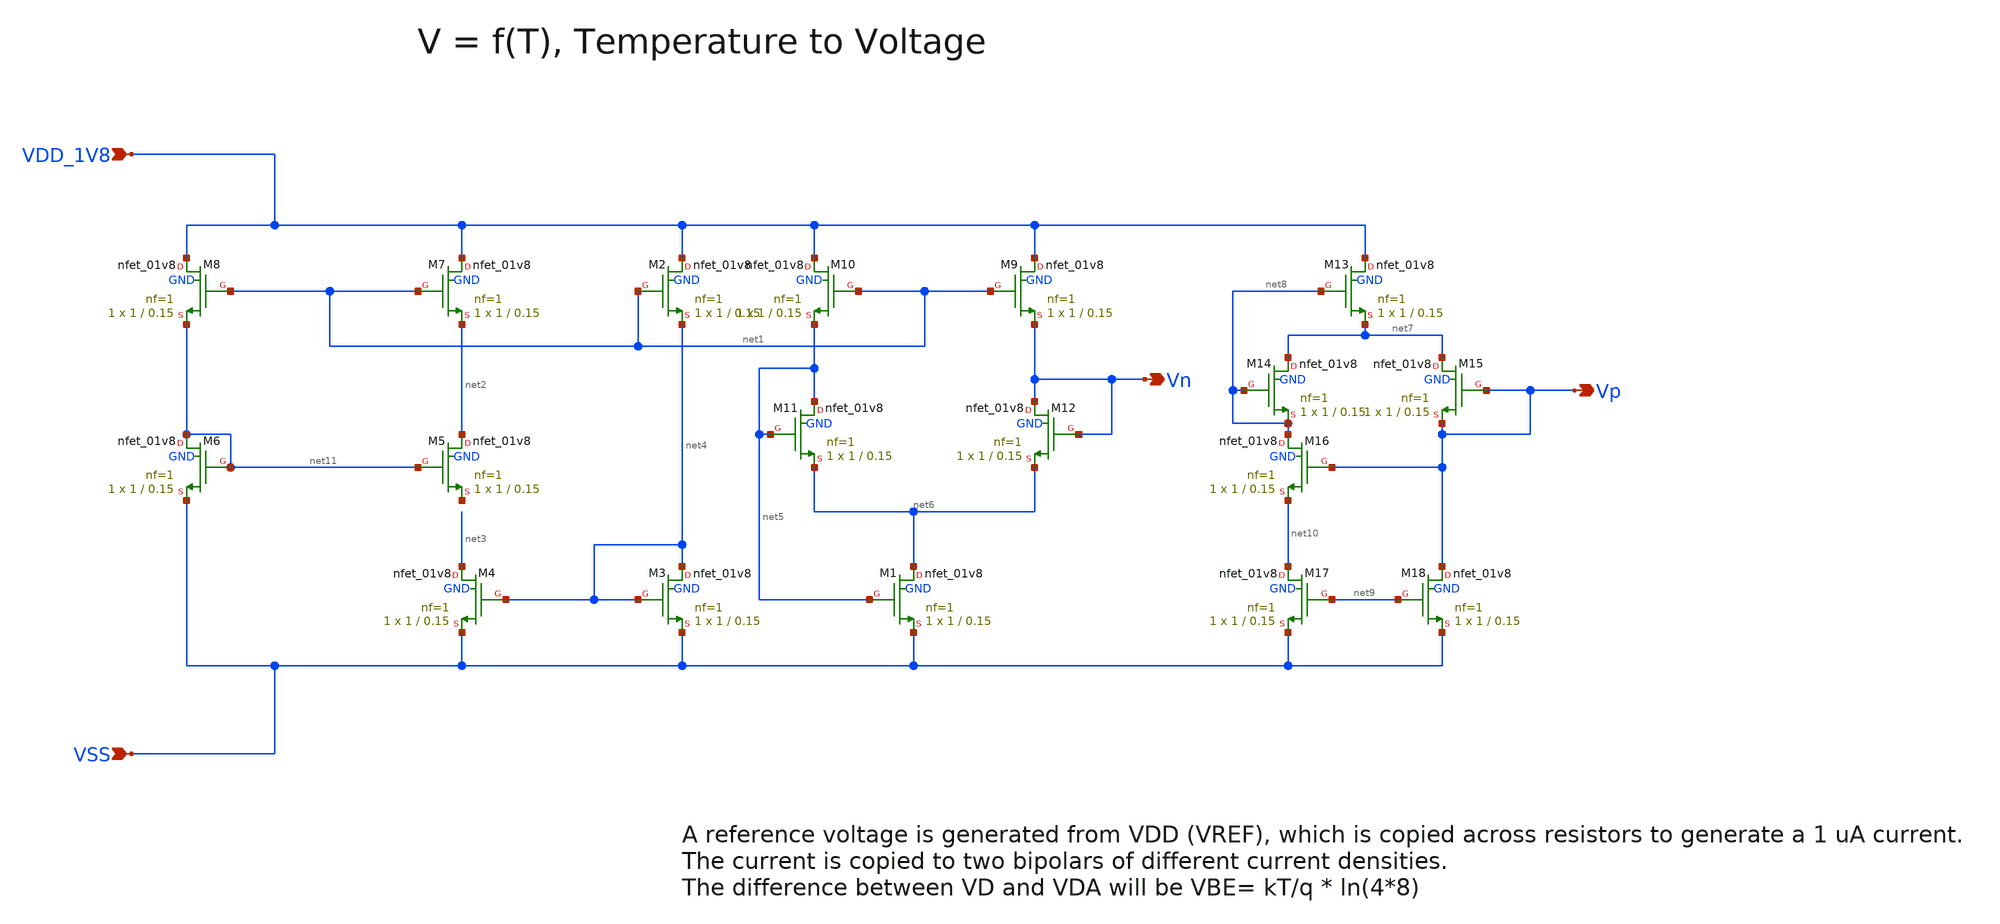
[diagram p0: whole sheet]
** sch_path: design/CNR_GR06_SKY130NM/CNR_GR06_test.sch
**.subckt CNR_GR06_test VDD_1V8 VSS Vn Vp
*.ipin VDD_1V8
*.ipin VSS
*.opin Vn
*.opin Vp
XM1 net6 net5 VSS GND sky130_fd_pr__nfet_01v8 L=0.15 W=1 nf=1 ad='int((nf+1)/2) * W/nf * 0.29' as='int((nf+2)/2) * W/nf * 0.29'
+ pd='2*int((nf+1)/2) * (W/nf + 0.29)' ps='2*int((nf+2)/2) * (W/nf + 0.29)' nrd='0.29 / W' nrs='0.29 / W'
+ sa=0 sb=0 sd=0 mult=1 m=1
XM3 net4 net4 VSS GND sky130_fd_pr__nfet_01v8 L=0.15 W=1 nf=1 ad='int((nf+1)/2) * W/nf * 0.29' as='int((nf+2)/2) * W/nf * 0.29'
+ pd='2*int((nf+1)/2) * (W/nf + 0.29)' ps='2*int((nf+2)/2) * (W/nf + 0.29)' nrd='0.29 / W' nrs='0.29 / W'
+ sa=0 sb=0 sd=0 mult=1 m=1
XM4 net3 net4 VSS GND sky130_fd_pr__nfet_01v8 L=0.15 W=1 nf=1 ad='int((nf+1)/2) * W/nf * 0.29' as='int((nf+2)/2) * W/nf * 0.29'
+ pd='2*int((nf+1)/2) * (W/nf + 0.29)' ps='2*int((nf+2)/2) * (W/nf + 0.29)' nrd='0.29 / W' nrs='0.29 / W'
+ sa=0 sb=0 sd=0 mult=1 m=1
XM5 net2 net11 net12 GND sky130_fd_pr__nfet_01v8 L=0.15 W=1 nf=1 ad='int((nf+1)/2) * W/nf * 0.29' as='int((nf+2)/2) * W/nf * 0.29'
+ pd='2*int((nf+1)/2) * (W/nf + 0.29)' ps='2*int((nf+2)/2) * (W/nf + 0.29)' nrd='0.29 / W' nrs='0.29 / W'
+ sa=0 sb=0 sd=0 mult=1 m=1
XM6 net11 net11 VSS GND sky130_fd_pr__nfet_01v8 L=0.15 W=1 nf=1 ad='int((nf+1)/2) * W/nf * 0.29' as='int((nf+2)/2) * W/nf * 0.29'
+ pd='2*int((nf+1)/2) * (W/nf + 0.29)' ps='2*int((nf+2)/2) * (W/nf + 0.29)' nrd='0.29 / W' nrs='0.29 / W'
+ sa=0 sb=0 sd=0 mult=1 m=1
XM11 net5 net5 net6 GND sky130_fd_pr__nfet_01v8 L=0.15 W=1 nf=1 ad='int((nf+1)/2) * W/nf * 0.29' as='int((nf+2)/2) * W/nf * 0.29'
+ pd='2*int((nf+1)/2) * (W/nf + 0.29)' ps='2*int((nf+2)/2) * (W/nf + 0.29)' nrd='0.29 / W' nrs='0.29 / W'
+ sa=0 sb=0 sd=0 mult=1 m=1
XM12 Vn Vn net6 GND sky130_fd_pr__nfet_01v8 L=0.15 W=1 nf=1 ad='int((nf+1)/2) * W/nf * 0.29' as='int((nf+2)/2) * W/nf * 0.29'
+ pd='2*int((nf+1)/2) * (W/nf + 0.29)' ps='2*int((nf+2)/2) * (W/nf + 0.29)' nrd='0.29 / W' nrs='0.29 / W'
+ sa=0 sb=0 sd=0 mult=1 m=1
XM17 net10 net9 VSS GND sky130_fd_pr__nfet_01v8 L=0.15 W=1 nf=1 ad='int((nf+1)/2) * W/nf * 0.29' as='int((nf+2)/2) * W/nf * 0.29'
+ pd='2*int((nf+1)/2) * (W/nf + 0.29)' ps='2*int((nf+2)/2) * (W/nf + 0.29)' nrd='0.29 / W' nrs='0.29 / W'
+ sa=0 sb=0 sd=0 mult=1 m=1
XM18 Vp net9 VSS GND sky130_fd_pr__nfet_01v8 L=0.15 W=1 nf=1 ad='int((nf+1)/2) * W/nf * 0.29' as='int((nf+2)/2) * W/nf * 0.29'
+ pd='2*int((nf+1)/2) * (W/nf + 0.29)' ps='2*int((nf+2)/2) * (W/nf + 0.29)' nrd='0.29 / W' nrs='0.29 / W'
+ sa=0 sb=0 sd=0 mult=1 m=1
XM8 VDD_1V8 net1 net11 GND sky130_fd_pr__nfet_01v8 L=0.15 W=1 nf=1 ad='int((nf+1)/2) * W/nf * 0.29' as='int((nf+2)/2) * W/nf * 0.29'
+ pd='2*int((nf+1)/2) * (W/nf + 0.29)' ps='2*int((nf+2)/2) * (W/nf + 0.29)' nrd='0.29 / W' nrs='0.29 / W'
+ sa=0 sb=0 sd=0 mult=1 m=1
XM7 VDD_1V8 net1 net2 GND sky130_fd_pr__nfet_01v8 L=0.15 W=1 nf=1 ad='int((nf+1)/2) * W/nf * 0.29' as='int((nf+2)/2) * W/nf * 0.29'
+ pd='2*int((nf+1)/2) * (W/nf + 0.29)' ps='2*int((nf+2)/2) * (W/nf + 0.29)' nrd='0.29 / W' nrs='0.29 / W'
+ sa=0 sb=0 sd=0 mult=1 m=1
XM2 VDD_1V8 net1 net4 GND sky130_fd_pr__nfet_01v8 L=0.15 W=1 nf=1 ad='int((nf+1)/2) * W/nf * 0.29' as='int((nf+2)/2) * W/nf * 0.29'
+ pd='2*int((nf+1)/2) * (W/nf + 0.29)' ps='2*int((nf+2)/2) * (W/nf + 0.29)' nrd='0.29 / W' nrs='0.29 / W'
+ sa=0 sb=0 sd=0 mult=1 m=1
XM10 VDD_1V8 net1 net5 GND sky130_fd_pr__nfet_01v8 L=0.15 W=1 nf=1 ad='int((nf+1)/2) * W/nf * 0.29' as='int((nf+2)/2) * W/nf * 0.29'
+ pd='2*int((nf+1)/2) * (W/nf + 0.29)' ps='2*int((nf+2)/2) * (W/nf + 0.29)' nrd='0.29 / W' nrs='0.29 / W'
+ sa=0 sb=0 sd=0 mult=1 m=1
XM9 VDD_1V8 net1 Vn GND sky130_fd_pr__nfet_01v8 L=0.15 W=1 nf=1 ad='int((nf+1)/2) * W/nf * 0.29' as='int((nf+2)/2) * W/nf * 0.29'
+ pd='2*int((nf+1)/2) * (W/nf + 0.29)' ps='2*int((nf+2)/2) * (W/nf + 0.29)' nrd='0.29 / W' nrs='0.29 / W'
+ sa=0 sb=0 sd=0 mult=1 m=1
XM13 VDD_1V8 net8 net7 GND sky130_fd_pr__nfet_01v8 L=0.15 W=1 nf=1 ad='int((nf+1)/2) * W/nf * 0.29' as='int((nf+2)/2) * W/nf * 0.29'
+ pd='2*int((nf+1)/2) * (W/nf + 0.29)' ps='2*int((nf+2)/2) * (W/nf + 0.29)' nrd='0.29 / W' nrs='0.29 / W'
+ sa=0 sb=0 sd=0 mult=1 m=1
XM15 net7 Vp Vp GND sky130_fd_pr__nfet_01v8 L=0.15 W=1 nf=1 ad='int((nf+1)/2) * W/nf * 0.29' as='int((nf+2)/2) * W/nf * 0.29'
+ pd='2*int((nf+1)/2) * (W/nf + 0.29)' ps='2*int((nf+2)/2) * (W/nf + 0.29)' nrd='0.29 / W' nrs='0.29 / W'
+ sa=0 sb=0 sd=0 mult=1 m=1
XM14 net7 net8 net8 GND sky130_fd_pr__nfet_01v8 L=0.15 W=1 nf=1 ad='int((nf+1)/2) * W/nf * 0.29' as='int((nf+2)/2) * W/nf * 0.29'
+ pd='2*int((nf+1)/2) * (W/nf + 0.29)' ps='2*int((nf+2)/2) * (W/nf + 0.29)' nrd='0.29 / W' nrs='0.29 / W'
+ sa=0 sb=0 sd=0 mult=1 m=1
XM16 net8 Vp net10 GND sky130_fd_pr__nfet_01v8 L=0.15 W=1 nf=1 ad='int((nf+1)/2) * W/nf * 0.29' as='int((nf+2)/2) * W/nf * 0.29'
+ pd='2*int((nf+1)/2) * (W/nf + 0.29)' ps='2*int((nf+2)/2) * (W/nf + 0.29)' nrd='0.29 / W' nrs='0.29 / W'
+ sa=0 sb=0 sd=0 mult=1 m=1
**.ends
.end
